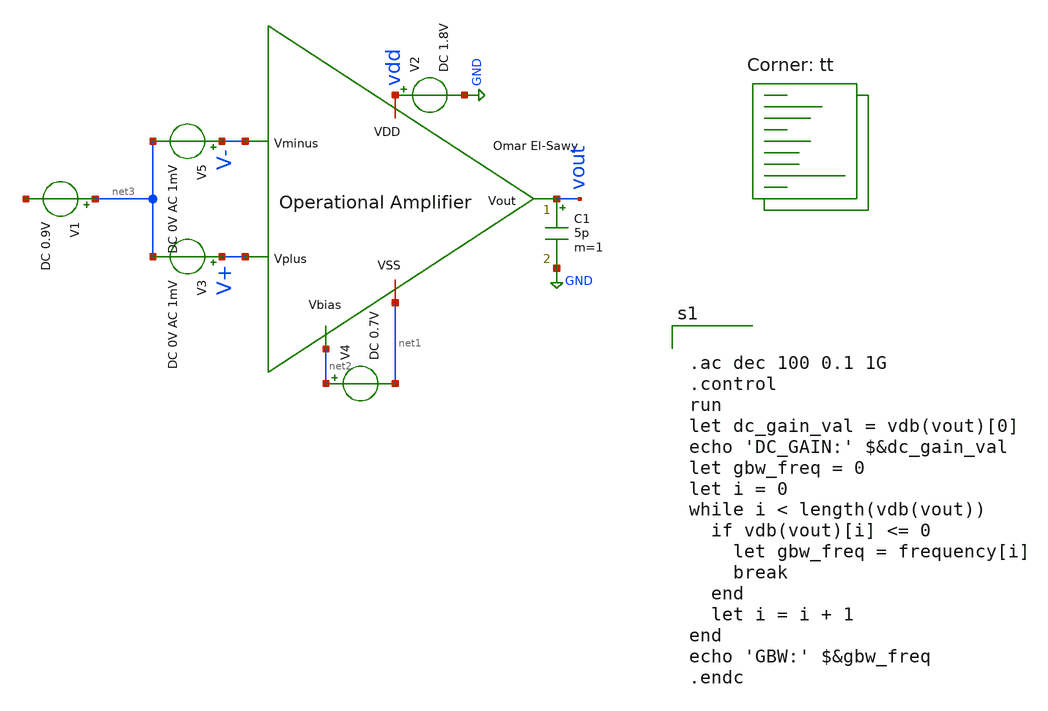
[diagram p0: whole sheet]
** sch_path: analog/library/OpAmps/template/OpAmp_tb.sch
**.subckt OpAmp_tb
x1 vdd vout V- V+ net2 net1 OpAmp
V1 net3 net4 DC 0.9V
V2 vdd GND DC 1.8V
V4 net2 net1 DC 0.7V
C1 vout GND 5p m=1
V3 V+ net3 DC 0V AC 1mV
V5 V- net3 DC 0V AC 1mV
**** begin user architecture code


.ac dec 100 0.1 1G
.control
run
let dc_gain_val = vdb(vout)[0]
echo 'DC_GAIN:' $&dc_gain_val
let gbw_freq = 0
let i = 0
while i < length(vdb(vout))
  if vdb(vout)[i] <= 0
    let gbw_freq = frequency[i]
    break
  end
  let i = i + 1
end
echo 'GBW:' $&gbw_freq
.endc


.lib $::SKYWATER_MODELS/sky130.lib.spice tt
**** end user architecture code
**.ends

* expanding   symbol:  OpAmps/template/OpAmp.sym # of pins=6
** sym_path: OpAmps/template/OpAmp.sym
** sch_path: OpAmps/template/OpAmp.sch
.subckt OpAmp VDD Vout Vminus Vplus Vbias VSS
*.ipin Vplus
*.ipin Vminus
*.iopin VDD
*.iopin VSS
*.ipin Vbias
*.opin Vout
XM1 net2 Vminus net1 VSS sky130_fd_pr__nfet_01v8 L=0.15 W=16 nf=1 ad='int((nf+1)/2) * W/nf * 0.29' as='int((nf+2)/2) * W/nf * 0.29'
+ pd='2*int((nf+1)/2) * (W/nf + 0.29)' ps='2*int((nf+2)/2) * (W/nf + 0.29)' nrd='0.29 / W' nrs='0.29 / W'
+ sa=0 sb=0 sd=0 mult=1 m=1
XM2 net3 Vplus net1 VSS sky130_fd_pr__nfet_01v8 L=0.15 W=16 nf=1 ad='int((nf+1)/2) * W/nf * 0.29' as='int((nf+2)/2) * W/nf * 0.29'
+ pd='2*int((nf+1)/2) * (W/nf + 0.29)' ps='2*int((nf+2)/2) * (W/nf + 0.29)' nrd='0.29 / W' nrs='0.29 / W'
+ sa=0 sb=0 sd=0 mult=1 m=1
XM3 net2 net2 VDD VDD sky130_fd_pr__pfet_01v8 L=0.4 W=1 nf=1 ad='int((nf+1)/2) * W/nf * 0.29' as='int((nf+2)/2) * W/nf * 0.29'
+ pd='2*int((nf+1)/2) * (W/nf + 0.29)' ps='2*int((nf+2)/2) * (W/nf + 0.29)' nrd='0.29 / W' nrs='0.29 / W'
+ sa=0 sb=0 sd=0 mult=1 m=1
XM4 net3 net2 VDD VDD sky130_fd_pr__pfet_01v8 L=0.4 W=1 nf=1 ad='int((nf+1)/2) * W/nf * 0.29' as='int((nf+2)/2) * W/nf * 0.29'
+ pd='2*int((nf+1)/2) * (W/nf + 0.29)' ps='2*int((nf+2)/2) * (W/nf + 0.29)' nrd='0.29 / W' nrs='0.29 / W'
+ sa=0 sb=0 sd=0 mult=1 m=1
XM5 net1 Vbias VSS VSS sky130_fd_pr__nfet_01v8 L=0.30 W=2 nf=1 ad='int((nf+1)/2) * W/nf * 0.29' as='int((nf+2)/2) * W/nf * 0.29'
+ pd='2*int((nf+1)/2) * (W/nf + 0.29)' ps='2*int((nf+2)/2) * (W/nf + 0.29)' nrd='0.29 / W' nrs='0.29 / W'
+ sa=0 sb=0 sd=0 mult=1 m=1
XM6 Vout net3 VDD VDD sky130_fd_pr__pfet_01v8 L=0.40 W=1 nf=1 ad='int((nf+1)/2) * W/nf * 0.29' as='int((nf+2)/2) * W/nf * 0.29'
+ pd='2*int((nf+1)/2) * (W/nf + 0.29)' ps='2*int((nf+2)/2) * (W/nf + 0.29)' nrd='0.29 / W' nrs='0.29 / W'
+ sa=0 sb=0 sd=0 mult=1 m=1
XC1 Vout net3 sky130_fd_pr__cap_mim_m3_1 W=1 L=1 MF=1 m=1
XM7 Vout Vbias VSS VSS sky130_fd_pr__nfet_01v8 L=0.3 W=1 nf=1 ad='int((nf+1)/2) * W/nf * 0.29' as='int((nf+2)/2) * W/nf * 0.29'
+ pd='2*int((nf+1)/2) * (W/nf + 0.29)' ps='2*int((nf+2)/2) * (W/nf + 0.29)' nrd='0.29 / W' nrs='0.29 / W'
+ sa=0 sb=0 sd=0 mult=1 m=1
.ends

.GLOBAL GND
.GLOBAL VDD
.GLOBAL VSS
.end
